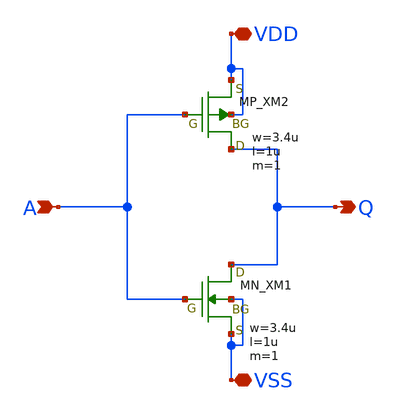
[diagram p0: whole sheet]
** sch_path: member_project/inverter_MUX/INV_05.sch
**.subckt INV_05 VSS A Q VDD
*.iopin VSS
*.ipin A
*.opin Q
*.iopin VDD
XM1 Q A VSS VSS NMOS w=3.4u l=1u as=0 ad=0 ps=0 pd=0 nrd=0 nrs=0 m=1
XM2 Q A VDD VDD PMOS w=3.4u l=1u as=0 ad=0 ps=0 pd=0 nrd=0 nrs=0 m=1
**.ends
.end
